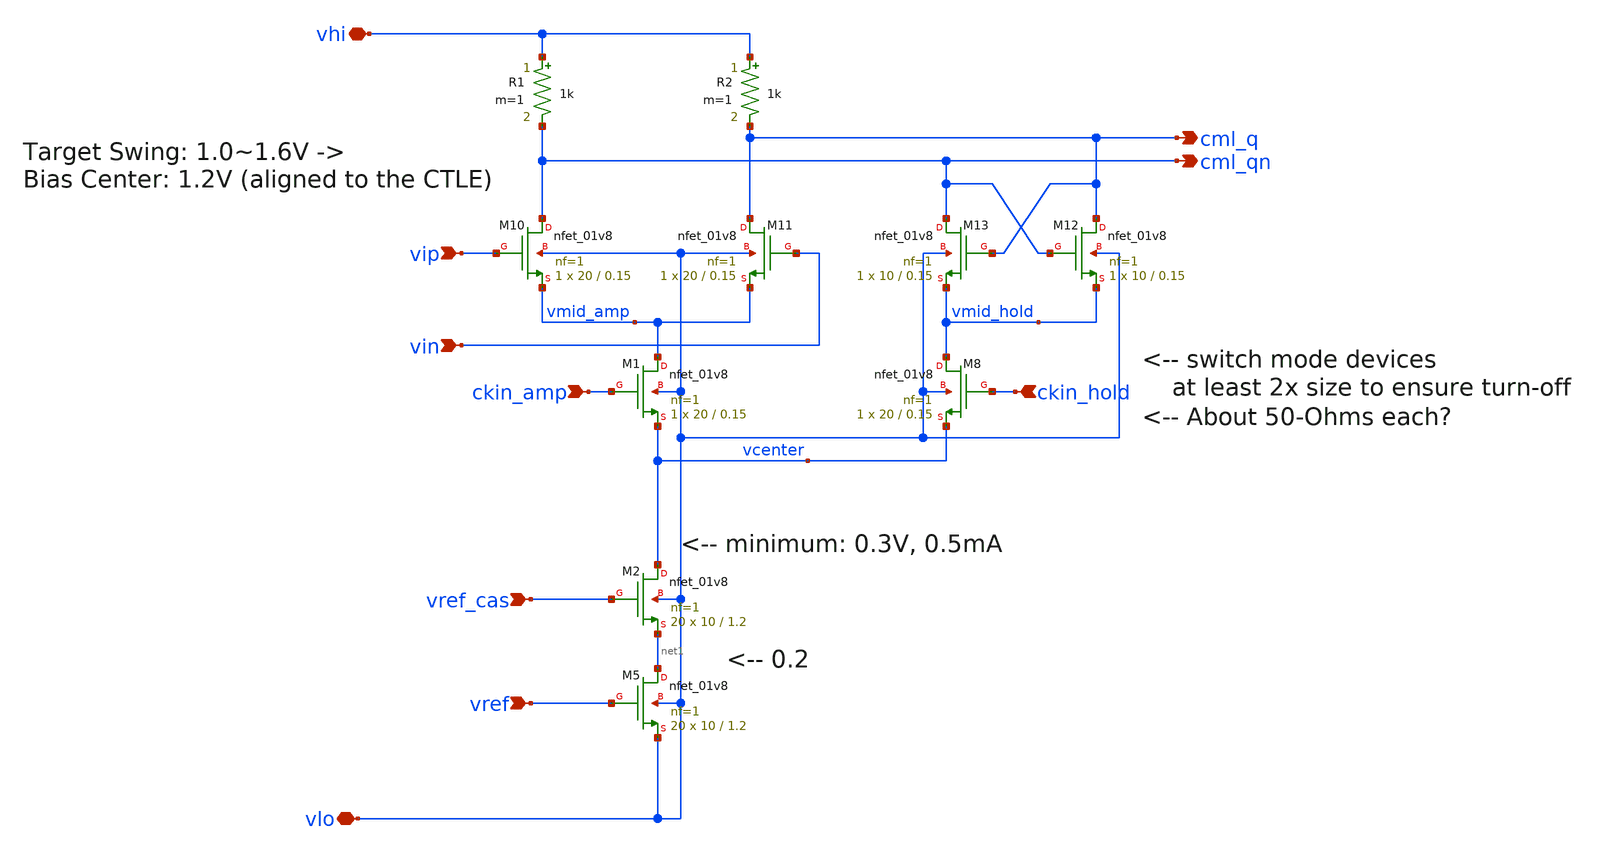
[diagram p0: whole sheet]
** sch_path: xschem/CML_latch_1mA.sch
**.subckt CML_latch_1mA cml_q cml_qn vhi ckin_amp ckin_hold vref_cas vref vlo vip vin
*.opin cml_q
*.opin cml_qn
*.iopin vhi
*.ipin ckin_amp
*.ipin ckin_hold
*.ipin vref_cas
*.ipin vref
*.iopin vlo
*.ipin vip
*.ipin vin
XM5 net1 vref vlo vlo sky130_fd_pr__nfet_01v8 L=1.2 W=10 nf=1 ad='int((nf+1)/2) * W/nf * 0.29' as='int((nf+2)/2) * W/nf * 0.29'
+ pd='2*int((nf+1)/2) * (W/nf + 0.29)' ps='2*int((nf+2)/2) * (W/nf + 0.29)' nrd='0.29 / W' nrs='0.29 / W'
+ sa=0 sb=0 sd=0 mult=20 m=20
XM2 vcenter vref_cas net1 vlo sky130_fd_pr__nfet_01v8 L=1.2 W=10 nf=1 ad='int((nf+1)/2) * W/nf * 0.29'
+ as='int((nf+2)/2) * W/nf * 0.29' pd='2*int((nf+1)/2) * (W/nf + 0.29)' ps='2*int((nf+2)/2) * (W/nf + 0.29)'
+ nrd='0.29 / W' nrs='0.29 / W' sa=0 sb=0 sd=0 mult=20 m=20
XM1 vmid_amp ckin_amp vcenter vlo sky130_fd_pr__nfet_01v8 L=0.15 W=20 nf=1 ad='int((nf+1)/2) * W/nf * 0.29'
+ as='int((nf+2)/2) * W/nf * 0.29' pd='2*int((nf+1)/2) * (W/nf + 0.29)' ps='2*int((nf+2)/2) * (W/nf + 0.29)'
+ nrd='0.29 / W' nrs='0.29 / W' sa=0 sb=0 sd=0 mult=1 m=1
XM8 vmid_hold ckin_hold vcenter vlo sky130_fd_pr__nfet_01v8 L=0.15 W=20 nf=1 ad='int((nf+1)/2) * W/nf * 0.29'
+ as='int((nf+2)/2) * W/nf * 0.29' pd='2*int((nf+1)/2) * (W/nf + 0.29)' ps='2*int((nf+2)/2) * (W/nf + 0.29)'
+ nrd='0.29 / W' nrs='0.29 / W' sa=0 sb=0 sd=0 mult=1 m=1
XM10 cml_qn vip vmid_amp vlo sky130_fd_pr__nfet_01v8 L=0.15 W=20 nf=1 ad='int((nf+1)/2) * W/nf * 0.29'
+ as='int((nf+2)/2) * W/nf * 0.29' pd='2*int((nf+1)/2) * (W/nf + 0.29)' ps='2*int((nf+2)/2) * (W/nf + 0.29)'
+ nrd='0.29 / W' nrs='0.29 / W' sa=0 sb=0 sd=0 mult=1 m=1
XM11 cml_q vin vmid_amp vlo sky130_fd_pr__nfet_01v8 L=0.15 W=20 nf=1 ad='int((nf+1)/2) * W/nf * 0.29'
+ as='int((nf+2)/2) * W/nf * 0.29' pd='2*int((nf+1)/2) * (W/nf + 0.29)' ps='2*int((nf+2)/2) * (W/nf + 0.29)'
+ nrd='0.29 / W' nrs='0.29 / W' sa=0 sb=0 sd=0 mult=1 m=1
XM12 cml_q cml_qn vmid_hold vlo sky130_fd_pr__nfet_01v8 L=0.15 W=10 nf=1 ad='int((nf+1)/2) * W/nf * 0.29'
+ as='int((nf+2)/2) * W/nf * 0.29' pd='2*int((nf+1)/2) * (W/nf + 0.29)' ps='2*int((nf+2)/2) * (W/nf + 0.29)'
+ nrd='0.29 / W' nrs='0.29 / W' sa=0 sb=0 sd=0 mult=1 m=1
XM13 cml_qn cml_q vmid_hold vlo sky130_fd_pr__nfet_01v8 L=0.15 W=10 nf=1 ad='int((nf+1)/2) * W/nf * 0.29'
+ as='int((nf+2)/2) * W/nf * 0.29' pd='2*int((nf+1)/2) * (W/nf + 0.29)' ps='2*int((nf+2)/2) * (W/nf + 0.29)'
+ nrd='0.29 / W' nrs='0.29 / W' sa=0 sb=0 sd=0 mult=1 m=1
R1 vhi cml_qn 1k m=1
R2 vhi cml_q 1k m=1
**.ends
.end
